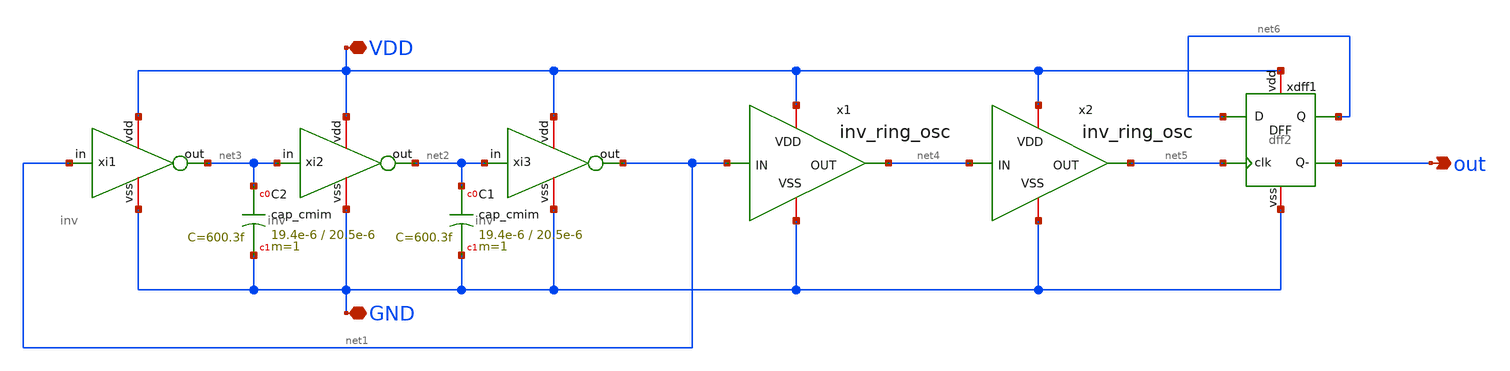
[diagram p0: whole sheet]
** sch_path: SSDOR_1.2V_v2/components/ring_osc/clk_ringosc.sch
**.subckt clk_ringosc GND VDD out
*.iopin GND
*.iopin VDD
*.opin out
xi1 VDD net1 net3 GND inv
xi2 VDD net3 net2 GND inv
xi3 VDD net2 net1 GND inv
x1 VDD net1 net4 GND inv_ring_osc
x2 VDD net4 net5 GND inv_ring_osc
XC2 net3 GND cap_cmim w=19.4e-6 l=20.5e-6 m=1 mm_ok=1
XC1 net2 GND cap_cmim w=19.4e-6 l=20.5e-6 m=1 mm_ok=1
xdff1 VDD net5 net6 net6 out GND dff2
**.ends
.end
